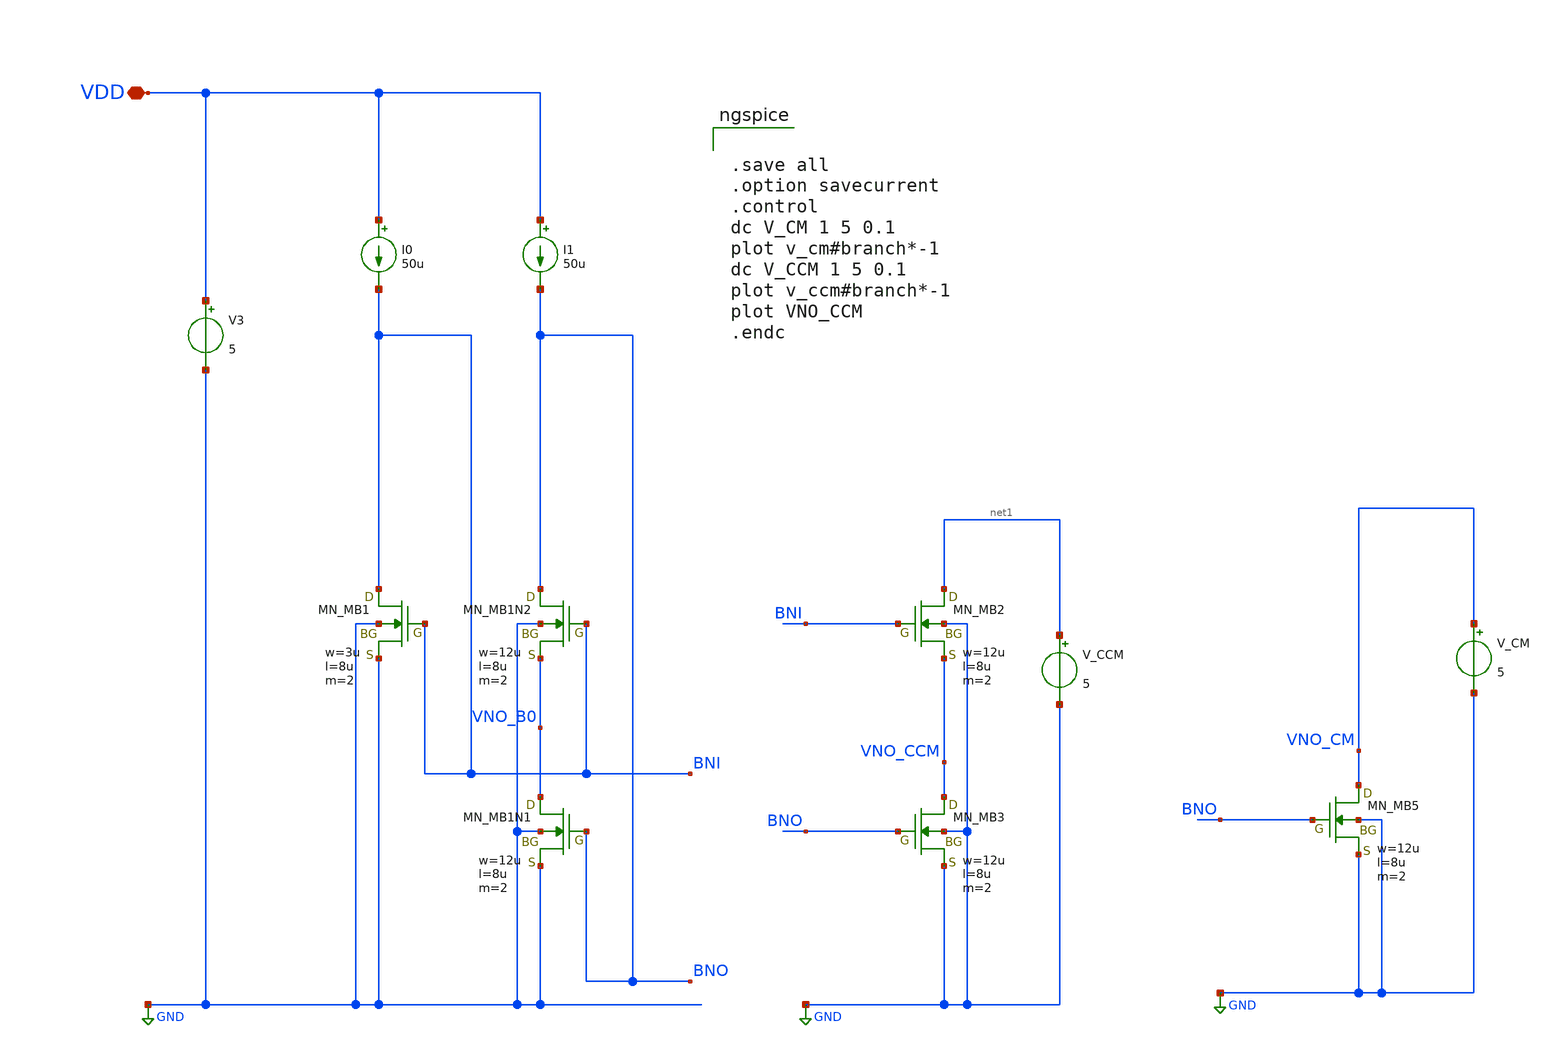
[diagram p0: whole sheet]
** sch_path: OpenSUSI-TR10/opamp_r2r/tb_lvccm.sch
**.subckt tb_lvccm VDD
*.iopin VDD
XMB1N2 BNO BNI VNO_B0 GND NMOS w=12u l=8u as=0 ad=0 ps=0 pd=0 nrd=0 nrs=0 m=2
XMB1N1 VNO_B0 BNO GND GND NMOS w=12u l=8u as=0 ad=0 ps=0 pd=0 nrd=0 nrs=0 m=2
XMB1 BNI BNI GND GND NMOS w=3u l=8u as=0 ad=0 ps=0 pd=0 nrd=0 nrs=0 m=2
I0 VDD BNI 50u
I1 VDD BNO 50u
XMB2 net1 BNI VNO_CCM GND NMOS w=12u l=8u as=0 ad=0 ps=0 pd=0 nrd=0 nrs=0 m=2
XMB3 VNO_CCM BNO GND GND NMOS w=12u l=8u as=0 ad=0 ps=0 pd=0 nrd=0 nrs=0 m=2
V_CCM net1 GND 5
XMB5 VNO_CM BNO GND GND NMOS w=12u l=8u as=0 ad=0 ps=0 pd=0 nrd=0 nrs=0 m=2
V_CM VNO_CM GND 5
V3 VDD GND 5
**** begin user architecture code

.save all
.option savecurrent
.control
dc V_CM 1 5 0.1
plot v_cm#branch*-1
dc V_CCM 1 5 0.1
plot v_ccm#branch*-1
plot VNO_CCM
.endc

 .include $::LIB/ip62_models
**** end user architecture code
**.ends
.GLOBAL GND
.end
